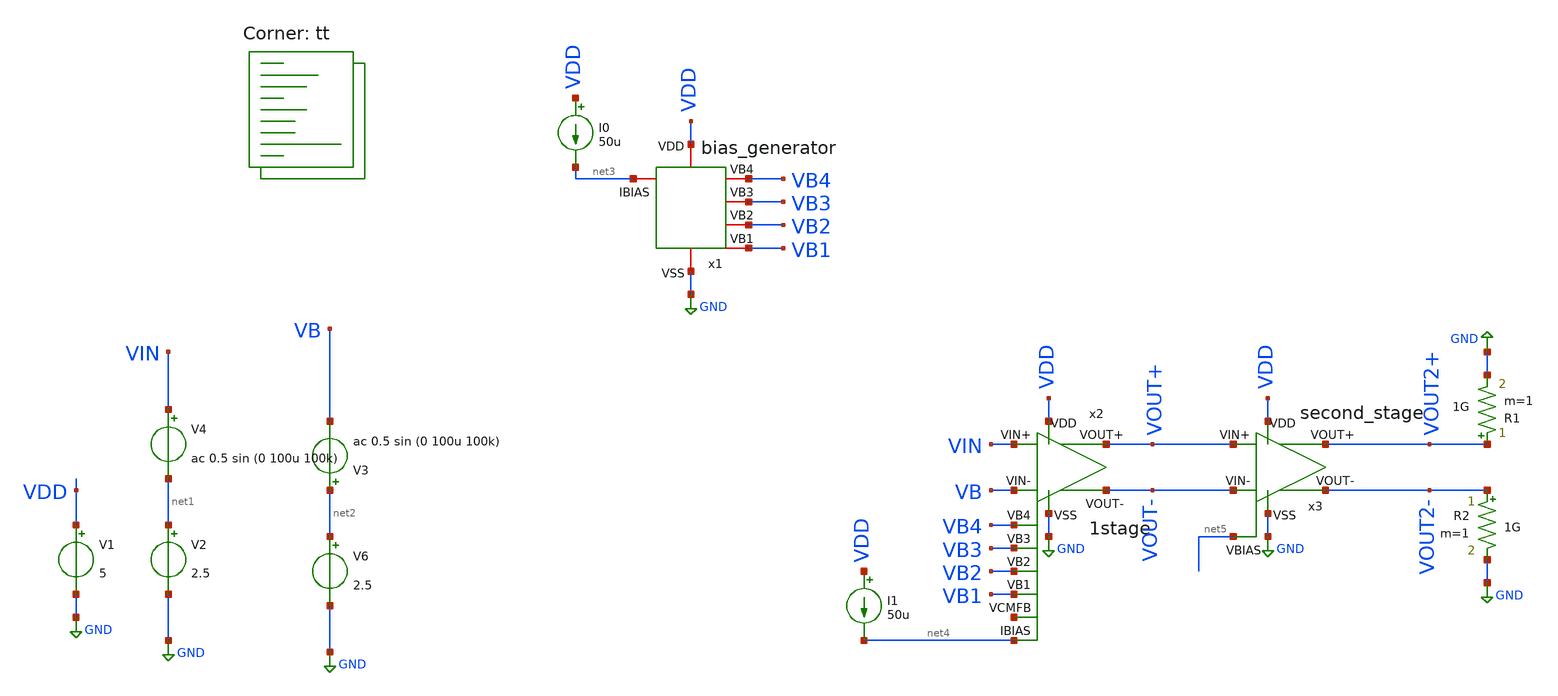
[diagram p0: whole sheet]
** sch_path: folded_cascode_amplifier/testbench/testbench.sch
**.subckt testbench
V1 VDD GND 5
V2 net1 GND 2.5
V6 net2 GND 2.5
V4 VIN net1 ac 0.5 sin (0 100u 100k)
V3 net2 VB ac 0.5 sin (0 100u 100k)
x1 net3 VDD GND VB4 VB3 VB2 VB1 bias_generator
I0 VDD net3 50u
x2 net4 VDD GND VB4 VB3 VB2 VB1 VOUT+ VOUT- VIN VB net6 1stage
I1 VDD net4 50u
R1 VOUT2+ GND 1G m=1
R2 VOUT2- GND 1G m=1
x3 VDD GND VOUT+ VOUT- VOUT2+ VOUT2- net5 second_stage
**** begin user architecture code

**************************************************************
**************************************************************
**************************************************************
**************************************************************
**************************************************************
*LIBs*********************************************************
**************************************************************
**************************************************************
**************************************************************
**************************************************************
**************************************************************
*.lib $::SKYWATER_MODELS/sky130.lib.spice tt
* chose the corners in the corner file
* tt_mm for mismatch
* ss ff sf fs standart corners
* ll hh lh hl capacitor and resistors corners
* mc for total process variation including corners
**************************************************************
**************************************************************
**************************************************************
**************************************************************
**************************************************************
*Corners/montecarlo options***********************************
**************************************************************
**************************************************************
**************************************************************
**************************************************************
**************************************************************
.TEMP 27
**************************************************************
**************************************************************
**************************************************************
**************************************************************
*SIMULATION and Plots*****************************************
**************************************************************
**************************************************************
**************************************************************
**************************************************************
.control
save all
dc V2 0 5 0.001
plot v(VOUT+) v(VOUT-) deriv(v(VOUT+)) deriv(v(VOUT-))
plot v(VOUT2+) v(VOUT2-) deriv(v(VOUT2+)) deriv(v(VOUT2-))
*plot v(VA)
*plot i(Vmeas)
ac dec 20 1 1000G
plot db(v(VOUT+))
plot db(v(VOUT2+)) phase(v(VOUT2+))
.endc

.lib $::SKYWATER_MODELS/sky130.lib.spice tt
**** end user architecture code
**.ends

* expanding   symbol:
*+  /home/vasco/Desktop/sky130A/folded_cascode_amplifier/Low_voltage_current_mirror_NMOS/bias_generator.sym # of pins=7
** sym_path: folded_cascode_amplifier/Low_voltage_current_mirror_NMOS/bias_generator.sym
** sch_path: folded_cascode_amplifier/Low_voltage_current_mirror_NMOS/bias_generator.sch
.subckt bias_generator IBIAS VDD VSS VB4 VB3 VB2 VB1
*.iopin IBIAS
*.iopin VDD
*.iopin VB4
*.iopin VB3
*.iopin VB2
*.iopin VB1
*.iopin VSS
XM5 VB1 VB2 net1 VSS sky130_fd_pr__nfet_g5v0d10v5 L=1.5 W=30 nf=1 ad='int((1 + 1)/2) * 30 / 1 * 0.29'
+ as='int((1 + 2)/2) * 30 / 1 * 0.29' pd='2*int((1 + 1)/2) * (30 / 1 + 0.29)' ps='2*int((1 + 2)/2) * (30 / 1 + 0.29)'
+ nrd='0.29 / 30 ' nrs='0.29 / 30 ' sa=0 sb=0 sd=0 mult=1 m=1
XM1 net1 VB1 VSS VSS sky130_fd_pr__nfet_g5v0d10v5 L=1.8 W=10 nf=1 ad='int((1 + 1)/2) * 10 / 1 * 0.29'
+ as='int((1 + 2)/2) * 10 / 1 * 0.29' pd='2*int((1 + 1)/2) * (10 / 1 + 0.29)' ps='2*int((1 + 2)/2) * (10 / 1 + 0.29)'
+ nrd='0.29 / 10 ' nrs='0.29 / 10 ' sa=0 sb=0 sd=0 mult=1 m=1
XR7 VB1 VB2 VDD sky130_fd_pr__res_high_po_0p69 L=1*20 mult=1 m=1
XM2 VB3 VB2 net2 VSS sky130_fd_pr__nfet_g5v0d10v5 L=1.5 W=30 nf=1 ad='int((1 + 1)/2) * 30 / 1 * 0.29'
+ as='int((1 + 2)/2) * 30 / 1 * 0.29' pd='2*int((1 + 1)/2) * (30 / 1 + 0.29)' ps='2*int((1 + 2)/2) * (30 / 1 + 0.29)'
+ nrd='0.29 / 30 ' nrs='0.29 / 30 ' sa=0 sb=0 sd=0 mult=1 m=1
XM3 net2 VB1 VSS VSS sky130_fd_pr__nfet_g5v0d10v5 L=1.8 W=10 nf=1 ad='int((1 + 1)/2) * 10 / 1 * 0.29'
+ as='int((1 + 2)/2) * 10 / 1 * 0.29' pd='2*int((1 + 1)/2) * (10 / 1 + 0.29)' ps='2*int((1 + 2)/2) * (10 / 1 + 0.29)'
+ nrd='0.29 / 10 ' nrs='0.29 / 10 ' sa=0 sb=0 sd=0 mult=1 m=1
XR1 VB3 VB4 VDD sky130_fd_pr__res_high_po_0p69 L=1*20 mult=1 m=1
XM9 VB4 VB3 net3 net3 sky130_fd_pr__pfet_g5v0d10v5 L=1.2 W=20 nf=1 ad='int((1 + 1)/2) * 20 / 1 * 0.29'
+ as='int((1 + 2)/2) * 20 / 1 * 0.29' pd='2*int((1 + 1)/2) * (20 / 1 + 0.29)' ps='2*int((1 + 2)/2) * (20 / 1 + 0.29)'
+ nrd='0.29 / 20 ' nrs='0.29 / 20 ' sa=0 sb=0 sd=0 mult=1 m=1
XM4 net3 VB4 VDD VDD sky130_fd_pr__pfet_g5v0d10v5 L=1.5 W=25 nf=1 ad='int((1 + 1)/2) * 25 / 1 * 0.29'
+ as='int((1 + 2)/2) * 25 / 1 * 0.29' pd='2*int((1 + 1)/2) * (25 / 1 + 0.29)' ps='2*int((1 + 2)/2) * (25 / 1 + 0.29)'
+ nrd='0.29 / 25 ' nrs='0.29 / 25 ' sa=0 sb=0 sd=0 mult=1 m=1
R2 IBIAS VB2 0.1 m=1
.ends


* expanding   symbol:  /home/vasco/Desktop/sky130A/folded_cascode_amplifier/1_stage/1stage.sym # of
*+ pins=12
** sym_path: folded_cascode_amplifier/1_stage/1stage.sym
** sch_path: folded_cascode_amplifier/1_stage/1stage.sch
.subckt 1stage IBIAS VDD VSS VB4 VB3 VB2 VB1 VOUT+ VOUT- VIN+ VIN- VCMFB
*.iopin IBIAS
*.iopin VDD
*.iopin VB4
*.iopin VB3
*.iopin VB2
*.iopin VB1
*.iopin VSS
*.iopin VOUT+
*.iopin VOUT-
*.iopin VIN+
*.iopin VIN-
*.iopin VCMFB
XM9 net3 VIN- net1 net1 sky130_fd_pr__pfet_g5v0d10v5 L=1 W=80 nf=1 ad='int((1 + 1)/2) * 80 / 1 * 0.29'
+ as='int((1 + 2)/2) * 80 / 1 * 0.29' pd='2*int((1 + 1)/2) * (80 / 1 + 0.29)' ps='2*int((1 + 2)/2) * (80 / 1 + 0.29)'
+ nrd='0.29 / 80 ' nrs='0.29 / 80 ' sa=0 sb=0 sd=0 mult=1 m=1
XM1 net2 VIN+ net1 net1 sky130_fd_pr__pfet_g5v0d10v5 L=1 W=80 nf=1 ad='int((1 + 1)/2) * 80 / 1 * 0.29'
+ as='int((1 + 2)/2) * 80 / 1 * 0.29' pd='2*int((1 + 1)/2) * (80 / 1 + 0.29)' ps='2*int((1 + 2)/2) * (80 / 1 + 0.29)'
+ nrd='0.29 / 80 ' nrs='0.29 / 80 ' sa=0 sb=0 sd=0 mult=1 m=1
R1 IBIAS net1 0.1 m=1
XM5 VOUT+ VB2 net2 VSS sky130_fd_pr__nfet_g5v0d10v5 L=1.2 W=25 nf=1 ad='int((1 + 1)/2) * 25 / 1 * 0.29'
+ as='int((1 + 2)/2) * 25 / 1 * 0.29' pd='2*int((1 + 1)/2) * (25 / 1 + 0.29)' ps='2*int((1 + 2)/2) * (25 / 1 + 0.29)'
+ nrd='0.29 / 25 ' nrs='0.29 / 25 ' sa=0 sb=0 sd=0 mult=1 m=1
XM2 net2 VB1 VSS VSS sky130_fd_pr__nfet_g5v0d10v5 L=1.5 W=20 nf=1 ad='int((1 + 1)/2) * 20 / 1 * 0.29'
+ as='int((1 + 2)/2) * 20 / 1 * 0.29' pd='2*int((1 + 1)/2) * (20 / 1 + 0.29)' ps='2*int((1 + 2)/2) * (20 / 1 + 0.29)'
+ nrd='0.29 / 20 ' nrs='0.29 / 20 ' sa=0 sb=0 sd=0 mult=1 m=1
XM3 VOUT- VB2 net3 VSS sky130_fd_pr__nfet_g5v0d10v5 L=1.2 W=25 nf=1 ad='int((1 + 1)/2) * 25 / 1 * 0.29'
+ as='int((1 + 2)/2) * 25 / 1 * 0.29' pd='2*int((1 + 1)/2) * (25 / 1 + 0.29)' ps='2*int((1 + 2)/2) * (25 / 1 + 0.29)'
+ nrd='0.29 / 25 ' nrs='0.29 / 25 ' sa=0 sb=0 sd=0 mult=1 m=1
XM4 net3 VB1 VSS VSS sky130_fd_pr__nfet_g5v0d10v5 L=1.5 W=20 nf=1 ad='int((1 + 1)/2) * 20 / 1 * 0.29'
+ as='int((1 + 2)/2) * 20 / 1 * 0.29' pd='2*int((1 + 1)/2) * (20 / 1 + 0.29)' ps='2*int((1 + 2)/2) * (20 / 1 + 0.29)'
+ nrd='0.29 / 20 ' nrs='0.29 / 20 ' sa=0 sb=0 sd=0 mult=1 m=1
XM6 VOUT+ VB3 net4 net4 sky130_fd_pr__pfet_g5v0d10v5 L=1.2 W=35 nf=1 ad='int((1 + 1)/2) * 35 / 1 * 0.29'
+ as='int((1 + 2)/2) * 35 / 1 * 0.29' pd='2*int((1 + 1)/2) * (35 / 1 + 0.29)' ps='2*int((1 + 2)/2) * (35 / 1 + 0.29)'
+ nrd='0.29 / 35 ' nrs='0.29 / 35 ' sa=0 sb=0 sd=0 mult=1 m=1
XM7 net4 VB4 VDD VDD sky130_fd_pr__pfet_g5v0d10v5 L=1.5 W=50 nf=1 ad='int((1 + 1)/2) * 50 / 1 * 0.29'
+ as='int((1 + 2)/2) * 50 / 1 * 0.29' pd='2*int((1 + 1)/2) * (50 / 1 + 0.29)' ps='2*int((1 + 2)/2) * (50 / 1 + 0.29)'
+ nrd='0.29 / 50 ' nrs='0.29 / 50 ' sa=0 sb=0 sd=0 mult=1 m=1
XM8 net5 VB4 VDD VDD sky130_fd_pr__pfet_g5v0d10v5 L=1.5 W=50 nf=1 ad='int((1 + 1)/2) * 50 / 1 * 0.29'
+ as='int((1 + 2)/2) * 50 / 1 * 0.29' pd='2*int((1 + 1)/2) * (50 / 1 + 0.29)' ps='2*int((1 + 2)/2) * (50 / 1 + 0.29)'
+ nrd='0.29 / 50 ' nrs='0.29 / 50 ' sa=0 sb=0 sd=0 mult=1 m=1
XM10 VOUT- VB3 net5 net5 sky130_fd_pr__pfet_g5v0d10v5 L=1.2 W=35 nf=1 ad='int((1 + 1)/2) * 35 / 1 * 0.29'
+ as='int((1 + 2)/2) * 35 / 1 * 0.29' pd='2*int((1 + 1)/2) * (35 / 1 + 0.29)' ps='2*int((1 + 2)/2) * (35 / 1 + 0.29)'
+ nrd='0.29 / 35 ' nrs='0.29 / 35 ' sa=0 sb=0 sd=0 mult=1 m=1
.ends


* expanding   symbol:  /home/vasco/Desktop/sky130A/folded_cascode_amplifier/2_stage/second_stage.sym
*+ # of pins=7
** sym_path: folded_cascode_amplifier/2_stage/second_stage.sym
** sch_path: folded_cascode_amplifier/2_stage/second_stage.sch
.subckt second_stage VDD VSS VIN+ VIN- VOUT+ VOUT- VBIAS
*.iopin VDD
*.iopin VSS
*.iopin VIN+
*.iopin VIN-
*.iopin VOUT+
*.iopin VOUT-
*.iopin VBIAS
XM5 VOUT+ VIN+ VSS VSS sky130_fd_pr__nfet_g5v0d10v5 L=1.5 W=20 nf=1 ad='int((1 + 1)/2) * 20 / 1 * 0.29'
+ as='int((1 + 2)/2) * 20 / 1 * 0.29' pd='2*int((1 + 1)/2) * (20 / 1 + 0.29)' ps='2*int((1 + 2)/2) * (20 / 1 + 0.29)'
+ nrd='0.29 / 20 ' nrs='0.29 / 20 ' sa=0 sb=0 sd=0 mult=1 m=1
XM1 VOUT- VIN- VSS VSS sky130_fd_pr__nfet_g5v0d10v5 L=1.5 W=20 nf=1 ad='int((1 + 1)/2) * 20 / 1 * 0.29'
+ as='int((1 + 2)/2) * 20 / 1 * 0.29' pd='2*int((1 + 1)/2) * (20 / 1 + 0.29)' ps='2*int((1 + 2)/2) * (20 / 1 + 0.29)'
+ nrd='0.29 / 20 ' nrs='0.29 / 20 ' sa=0 sb=0 sd=0 mult=1 m=1
XM9 VOUT+ VBIAS VDD VDD sky130_fd_pr__pfet_g5v0d10v5 L=1 W=60 nf=1 ad='int((1 + 1)/2) * 60 / 1 * 0.29'
+ as='int((1 + 2)/2) * 60 / 1 * 0.29' pd='2*int((1 + 1)/2) * (60 / 1 + 0.29)' ps='2*int((1 + 2)/2) * (60 / 1 + 0.29)'
+ nrd='0.29 / 60 ' nrs='0.29 / 60 ' sa=0 sb=0 sd=0 mult=1 m=1
XM2 VOUT- VBIAS VDD VDD sky130_fd_pr__pfet_g5v0d10v5 L=1 W=60 nf=1 ad='int((1 + 1)/2) * 60 / 1 * 0.29'
+ as='int((1 + 2)/2) * 60 / 1 * 0.29' pd='2*int((1 + 1)/2) * (60 / 1 + 0.29)' ps='2*int((1 + 2)/2) * (60 / 1 + 0.29)'
+ nrd='0.29 / 60 ' nrs='0.29 / 60 ' sa=0 sb=0 sd=0 mult=1 m=1
XR7 VIN+ net1 VDD sky130_fd_pr__res_high_po_0p69 L=500 mult=1 m=1
XC1 VOUT+ net1 sky130_fd_pr__cap_mim_m3_1 W=1 L=1 MF=1 m=1
XC2 VOUT- net2 sky130_fd_pr__cap_mim_m3_1 W=1 L=1 MF=1 m=1
XR1 VIN- net2 VDD sky130_fd_pr__res_high_po_0p69 L=500 mult=1 m=1
.ends

.GLOBAL GND
.end
